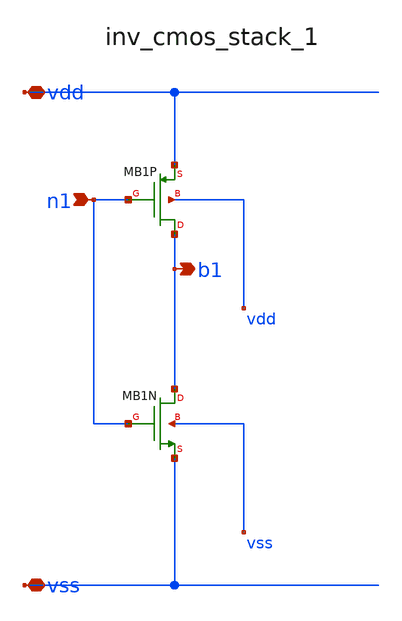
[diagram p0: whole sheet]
** sch_path: analog-db/raw/cmp_001_hyst_diffpair/hier/blocks/inv_cmos_stack_1.sch
**.subckt inv_cmos_stack_1 n1 vdd vss b1
*.ipin n1
*.iopin vdd
*.iopin vss
*.opin b1
XMB1N b1 n1 vss vss sg13_lv_nmos w=x_dut_xmb1n_w l=x_dut_xmb1n_l ng=1 m=x_dut_xmb1n_m
XMB1P b1 n1 vdd vdd sg13_lv_pmos w=x_dut_xmb1p_w l=x_dut_xmb1p_l ng=1 m=x_dut_xmb1p_m
**.ends
.end
